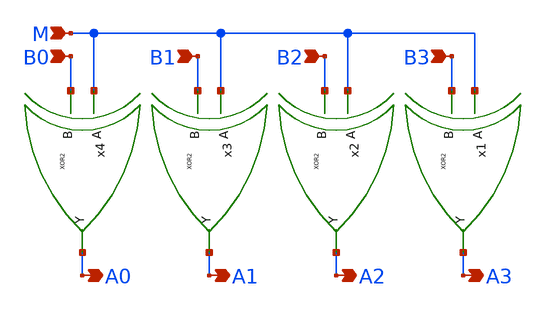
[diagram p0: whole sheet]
** sch_path: gates/4xorforsub.sch
**.subckt 4xorforsub B0 B1 B2 B3 A0 A1 A2 A3 M
*.ipin B0
*.ipin B1
*.ipin B2
*.ipin B3
*.opin A0
*.opin A1
*.opin A2
*.opin A3
*.ipin M
x1 M B3 A3 XOR2
x2 M B2 A2 XOR2
x3 M B1 A1 XOR2
x4 M B0 A0 XOR2
**.ends

* expanding   symbol:  XOR2.sym # of pins=3
** sym_path: gates/XOR2.sym
** sch_path: gates/XOR2.sch
.subckt XOR2 B A Y
*.ipin A
*.ipin B
*.opin Y
XM1 Y A net5 GND sky130_fd_pr__nfet_01v8 L=0.15 W=1 nf=1 ad='int((nf+1)/2) * W/nf * 0.29' as='int((nf+2)/2) * W/nf * 0.29'
+ pd='2*int((nf+1)/2) * (W/nf + 0.29)' ps='2*int((nf+2)/2) * (W/nf + 0.29)' nrd='0.29 / W' nrs='0.29 / W'
+ sa=0 sb=0 sd=0 mult=1 m=1
XM2 net5 B GND GND sky130_fd_pr__nfet_01v8 L=0.15 W=1 nf=1 ad='int((nf+1)/2) * W/nf * 0.29' as='int((nf+2)/2) * W/nf * 0.29'
+ pd='2*int((nf+1)/2) * (W/nf + 0.29)' ps='2*int((nf+2)/2) * (W/nf + 0.29)' nrd='0.29 / W' nrs='0.29 / W'
+ sa=0 sb=0 sd=0 mult=1 m=1
XM3 Y net1 net2 VDD sky130_fd_pr__pfet_01v8 L=0.15 W=1 nf=1 ad='int((nf+1)/2) * W/nf * 0.29' as='int((nf+2)/2) * W/nf * 0.29'
+ pd='2*int((nf+1)/2) * (W/nf + 0.29)' ps='2*int((nf+2)/2) * (W/nf + 0.29)' nrd='0.29 / W' nrs='0.29 / W'
+ sa=0 sb=0 sd=0 mult=1 m=1
XM4 net2 A VDD VDD sky130_fd_pr__pfet_01v8 L=0.15 W=1 nf=1 ad='int((nf+1)/2) * W/nf * 0.29' as='int((nf+2)/2) * W/nf * 0.29'
+ pd='2*int((nf+1)/2) * (W/nf + 0.29)' ps='2*int((nf+2)/2) * (W/nf + 0.29)' nrd='0.29 / W' nrs='0.29 / W'
+ sa=0 sb=0 sd=0 mult=1 m=1
XM5 net2 B VDD VDD sky130_fd_pr__pfet_01v8 L=0.15 W=1 nf=1 ad='int((nf+1)/2) * W/nf * 0.29' as='int((nf+2)/2) * W/nf * 0.29'
+ pd='2*int((nf+1)/2) * (W/nf + 0.29)' ps='2*int((nf+2)/2) * (W/nf + 0.29)' nrd='0.29 / W' nrs='0.29 / W'
+ sa=0 sb=0 sd=0 mult=1 m=1
XM6 Y net3 net2 VDD sky130_fd_pr__pfet_01v8 L=0.15 W=1 nf=1 ad='int((nf+1)/2) * W/nf * 0.29' as='int((nf+2)/2) * W/nf * 0.29'
+ pd='2*int((nf+1)/2) * (W/nf + 0.29)' ps='2*int((nf+2)/2) * (W/nf + 0.29)' nrd='0.29 / W' nrs='0.29 / W'
+ sa=0 sb=0 sd=0 mult=1 m=1
XM7 Y net1 net4 GND sky130_fd_pr__nfet_01v8 L=0.15 W=1 nf=1 ad='int((nf+1)/2) * W/nf * 0.29' as='int((nf+2)/2) * W/nf * 0.29'
+ pd='2*int((nf+1)/2) * (W/nf + 0.29)' ps='2*int((nf+2)/2) * (W/nf + 0.29)' nrd='0.29 / W' nrs='0.29 / W'
+ sa=0 sb=0 sd=0 mult=1 m=1
XM8 net4 net3 GND GND sky130_fd_pr__nfet_01v8 L=0.15 W=1 nf=1 ad='int((nf+1)/2) * W/nf * 0.29' as='int((nf+2)/2) * W/nf * 0.29'
+ pd='2*int((nf+1)/2) * (W/nf + 0.29)' ps='2*int((nf+2)/2) * (W/nf + 0.29)' nrd='0.29 / W' nrs='0.29 / W'
+ sa=0 sb=0 sd=0 mult=1 m=1
X1 A net1 inv_vtc
X2 B net3 inv_vtc
.ends


* expanding   symbol:  inv_vtc.sym # of pins=2
** sym_path: gates/inv_vtc.sym
** sch_path: gates/inv_vtc.sch
.subckt inv_vtc A Y
*.ipin A
*.opin Y
XM1 Y A VDD VDD sky130_fd_pr__pfet_01v8 L=0.15 W=2 nf=1 ad='int((nf+1)/2) * W/nf * 0.29' as='int((nf+2)/2) * W/nf * 0.29'
+ pd='2*int((nf+1)/2) * (W/nf + 0.29)' ps='2*int((nf+2)/2) * (W/nf + 0.29)' nrd='0.29 / W' nrs='0.29 / W'
+ sa=0 sb=0 sd=0 mult=1 m=1
XM2 Y A GND GND sky130_fd_pr__nfet_01v8 L=0.15 W=1 nf=1 ad='int((nf+1)/2) * W/nf * 0.29' as='int((nf+2)/2) * W/nf * 0.29'
+ pd='2*int((nf+1)/2) * (W/nf + 0.29)' ps='2*int((nf+2)/2) * (W/nf + 0.29)' nrd='0.29 / W' nrs='0.29 / W'
+ sa=0 sb=0 sd=0 mult=1 m=1
.ends

.GLOBAL VDD
.GLOBAL GND
.end
